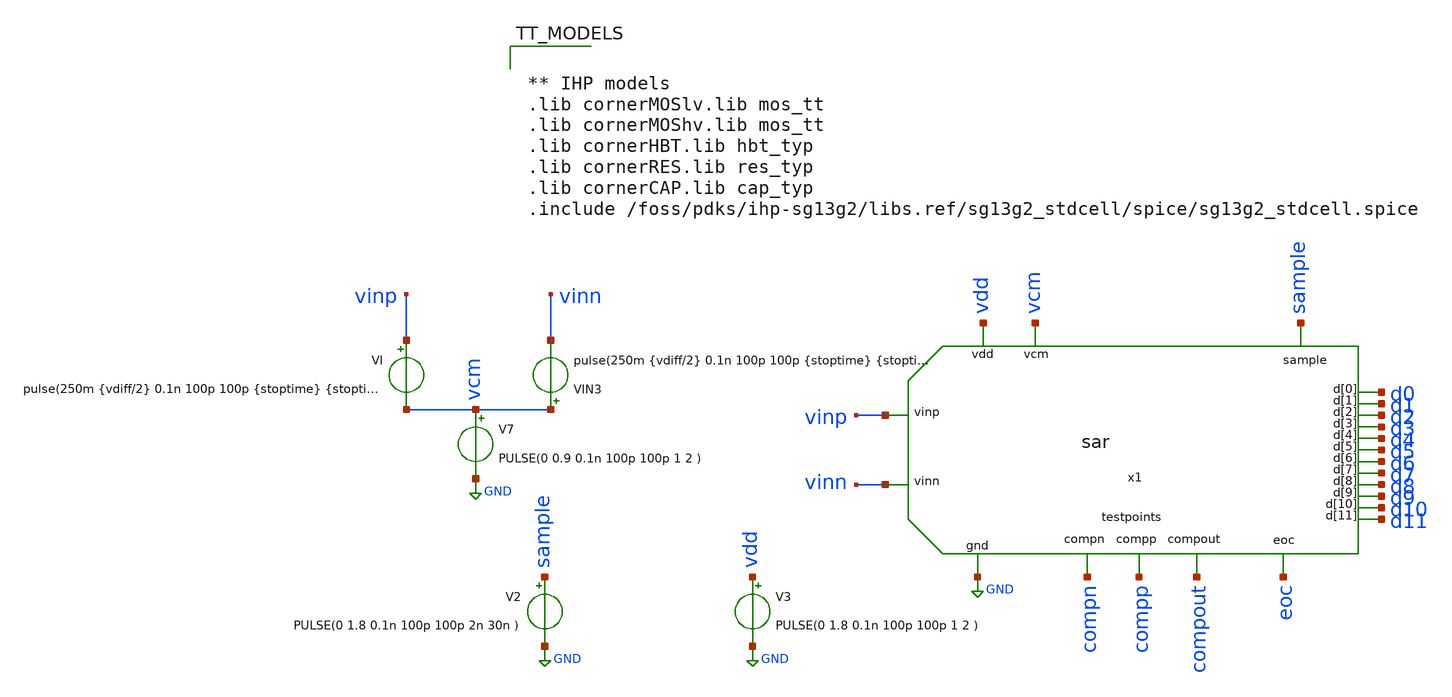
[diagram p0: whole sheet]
** sch_path: xschem/SAR_ADC/testbench/tb_sar_adc.sch
**.subckt tb_sar_adc
x1 vinp sample vinn GND vdd compn compp compout eoc d9 d7 d0 d11 d3 d4 d2 d1 d8 d6 d5 d10 vcm sar
VI vinp vcm pulse(250m {vdiff/2} 0.1n 100p 100p {stoptime} {stoptime+1} 1)
VIN3 vcm vinn pulse(250m {vdiff/2} 0.1n 100p 100p {stoptime} {stoptime+1} 1)
V2 sample GND PULSE(0 1.8 0.1n 100p 100p 2n 30n )
V3 vdd GND PULSE(0 1.8 0.1n 100p 100p 1 2 )
V7 vcm GND PULSE(0 0.9 0.1n 100p 100p 1 2 )
**** begin user architecture code


.param periodclk=1n
.param periodconv=20n
.param stoptime=1*periodconv
.param ro = 300

.param W_P = 1.0u
.param L_P = 0.13u
.param W_N = 1.0u
.param L_N = 0.13u

.param vdiff = 0.757

.options klu method=gear reltol=1e-2 abstol=1e-15 gmin=1e-15


.tran {0.005*periodclk} {stoptime}

.control

run

plot compp compn {compout + 4}
plot {d0} {d1 + 4} {d2 + 8} {d3 + 12} {d4 + 16} {d5 + 20} {d6 + 24} {d7 + 28} {d8 + 32} {d9 + 36} {d10 + 40}
+ {d11 + 44} {x1.comp_clk + 50} {compout + 55} {eoc + 60}  {compp - compn - 2}
plot compp-compn x1.comp_clk compout
plot sample eoc x1.x3.start

plot {(((V(d11)/1.8)*2048 + (V(d10)/1.8)*1024 + (V(d9)/1.8)*512 + (V(d8)/1.8)*256 + (V(d7)/1.8)*128 + (V(d6)/1.8)*64 + (V(d5)/1.8)*32 + (V(d4)/1.8)*16 + (V(d3)/1.8)*8 + (V(d2)/1.8)*4 + (V(d1)/1.8)*2 + (V(d0)/1.8)) - 2048) * 1.8/2048}
+ sample eoc vinp-vinn
plot {((((0-V(d11))/1.8)*2048 + (V(d10)/1.8)*1024 + (V(d9)/1.8)*512 + (V(d8)/1.8)*256 + (V(d7)/1.8)*128 + (V(d6)/1.8)*64 + (V(d5)/1.8)*32 + (V(d4)/1.8)*16 + (V(d3)/1.8)*8 + (V(d2)/1.8)*4 + (V(d1)/1.8)*2 + (V(d0)/1.8)) + 2048)*1.8/2048}
+ sample eoc vinp-vinn
*wrdata adc_signals.csv time V(d0) V(d1) V(d2) V(d3) V(d4) V(d5) V(d6) V(d7) V(d8) V(d9) V(d10)
*+ V(d11) vinp vinn eoc sample compout compp compn x1.comp_clk
*write adc_signals.raw time V(d0) V(d1) V(d2) V(d3) V(d4) V(d5) V(d6) V(d7) V(d8) V(d9) V(d10)
*+ V(d11) vinp vinn eoc sample compout compp compn x1.comp_clk
*quit
.endc




** IHP models
.lib cornerMOSlv.lib mos_tt
.lib cornerMOShv.lib mos_tt
.lib cornerHBT.lib hbt_typ
.lib cornerRES.lib res_typ
.lib cornerCAP.lib cap_typ
.include /foss/pdks/ihp-sg13g2/libs.ref/sg13g2_stdcell/spice/sg13g2_stdcell.spice


**** end user architecture code
**.ends
.GLOBAL GND
.end
